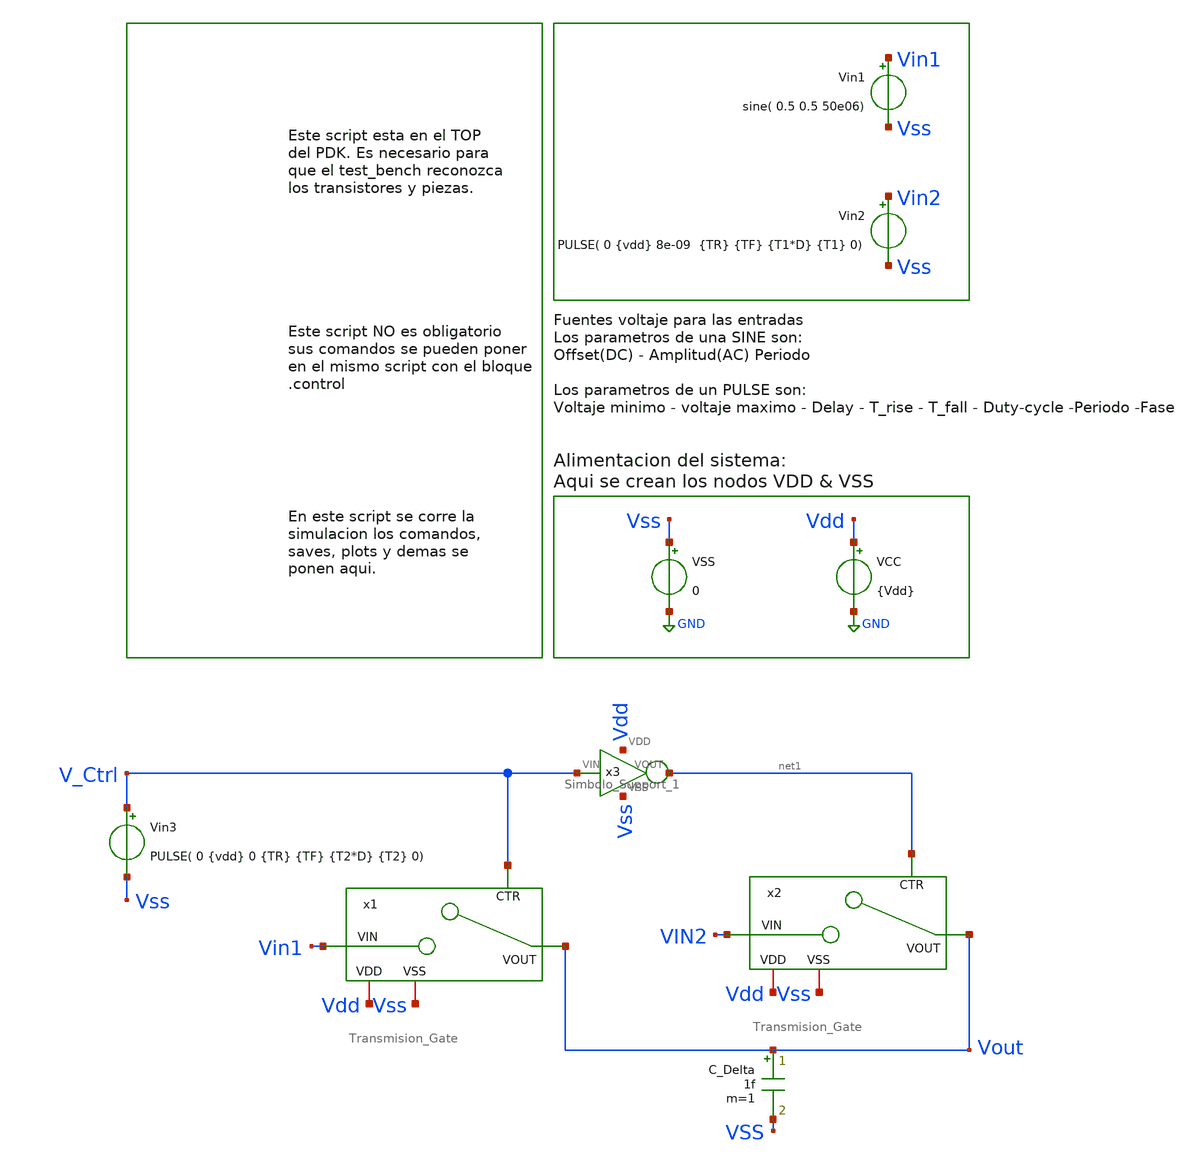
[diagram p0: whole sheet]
** sch_path: Taller2_extendido/Insumos/Transmision_Gate_Test_Solution.sch
**.subckt Transmision_Gate_Test_Solution
VCC Vdd GND {Vdd}
VSS Vss GND 0
Vin1 Vin1 Vss sine( 0.5 0.5 50e06)
Vin2 Vin2 Vss PULSE( 0 {vdd} 8e-09 {TR} {TF} {T1*D} {T1} 0)
C_Delta Vout VSS 1f m=1
Vin3 V_Ctrl Vss PULSE( 0 {vdd} 0 {TR} {TF} {T2*D} {T2} 0)
x3 Vdd V_Ctrl net1 Vss Simbolo_Support_1
x2 Vout VIN2 Vdd net1 Vss Transmision_Gate
x1 Vout Vin1 Vdd V_Ctrl Vss Transmision_Gate
**** begin user architecture code


.param corner=0

.if (corner==0)
.lib $::SG13G2_MODELS/cornerMOSlv.lib mos_tt
.lib $::SG13G2_MODELS/cornerMOSlv.lib mos_tt
.lib $::SG13G2_MODELS/cornerRES.lib res_typ
.lib $::SG13G2_MODELS/cornerCAP.lib cap_typ
.endif



.param Vdd = 1.2

.param temp = 27
.param TR = 240e-12
.param TF = 240e-12
.param D = 0.5
.param T2 = 200e-09
.param T1 = 15e-09





.save all

*.OPTION CSHUNT=0.05e-12
.OPTION ABSTOL=1e-15.
*.OPTION GMIN=1.0e-12.
.OPTION ITL1=1e5
*.OPTION RSHUNT=1e12
.OPTION RELTOL=1e-5


*Se guardan las transconductancias de compuerta Source-Drain
.save @n.x1.xm2.nsg13_lv_nmos[gds]
.save @n.x1.xm1.nsg13_lv_pmos[gds]
.save @n.x2.xm2.nsg13_lv_nmos[gds]
.save @n.x2.xm1.nsg13_lv_pmos[gds]

*Se guarda la tension Drain-source de los Mosfet en el Switch/Transmision-gate
.save @n.x1.xm2.nsg13_lv_nmos[vds]
.save @n.x1.xm1.nsg13_lv_pmos[vds]
.save @n.x2.xm2.nsg13_lv_nmos[vds]
.save @n.x2.xm1.nsg13_lv_pmos[vds]


.control
set color0 = white

tran 0.1n  400n

*Se convierten en variables transientes (poniendolas post sim tran) de variables guardadas
let GDS_N1 = @n.x1.xm2.nsg13_lv_nmos[gds]
let GDS_P1 = @n.x1.xm1.nsg13_lv_pmos[gds]
let GDS_N2 = @n.x2.xm2.nsg13_lv_nmos[gds]
let GDS_P2 = @n.x2.xm1.nsg13_lv_pmos[gds]

let Vds_N1 = @n.x1.xm2.nsg13_lv_nmos[vds]
let Vds_P1 = @n.x1.xm1.nsg13_lv_pmos[vds]
let Vds_N2 = @n.x2.xm2.nsg13_lv_nmos[vds]
let Vds_P2 = @n.x2.xm1.nsg13_lv_pmos[vds]

*Para guardar las resistencias de encendido se guarda como variable 1/gds:

let Ro_N1 = 1/GDS_N1
let Ro_P1 = 1/GDS_P1
let Ro_N2 = 1/GDS_N2
let Ro_P2 = 1/GDS_P2

*Plot salida basico
plot vout

*Plot salida en comparacion con la señal de control
plot V_ctrl+1.2 vout

*Opcionales para ver la diferencia de tension entre entrada y salida al TG. (Borral los * Para
*+ descomentar
*plot VIN1 vout
*plot VIN2 vout

*Plots de resistencias de encendido en cada transistor de los TG
plot Ro_P1 Ro_N1
plot Ro_N2 Ro_P2

*Plots de las diferencias de tension entre Drain y Source en cada MOS de los TG
plot Vds_N1 Vds_P1
plot Vds_N2 Vds_P2
plot Vds_P1
plot Vds_P2


.endc




**** end user architecture code
**.ends

* expanding   symbol:  /home/designer/shared/Taller2/Simbolo_Support_1.sym # of pins=4
** sym_path: Taller2_extendido/Insumos/Simbolo_Support_1.sym
** sch_path: Taller2_extendido/Insumos/Simbolo_Support_1.sch
.subckt Simbolo_Support_1 VDD VIN VOUT VSS
*.ipin VIN
*.iopin VDD
*.iopin VSS
*.opin VOUT
XM1 VOUT VIN VDD VDD sg13_lv_pmos w=1.0u l=0.15u ng=1 m=1 mm_ok=1
XM2 VOUT VIN VSS VSS sg13_lv_nmos w=1.0u l=0.15u ng=1 m=1 mm_ok=1
.ends


* expanding   symbol:  /home/designer/shared/Taller2/Transmision_Gate.sym # of pins=5
** sym_path: Taller2_extendido/Insumos/Transmision_Gate.sym
** sch_path: Taller2_extendido/Insumos/Transmision_Gate.sch
.subckt Transmision_Gate VOUT VIN VDD CTR VSS
*.ipin VIN
*.iopin VDD
*.iopin VSS
*.ipin CTR
*.opin VOUT
XM1 VOUT net1 VIN VDD sg13_lv_pmos w=6.0u l=0.15u ng=1 m=1 mm_ok=1
XM2 VOUT CTR VIN VSS sg13_lv_nmos w=2.0u l=0.15u ng=1 m=1 mm_ok=1
x1 VDD CTR net1 VSS Simbolo_Support_1
.ends

.GLOBAL GND
.end
